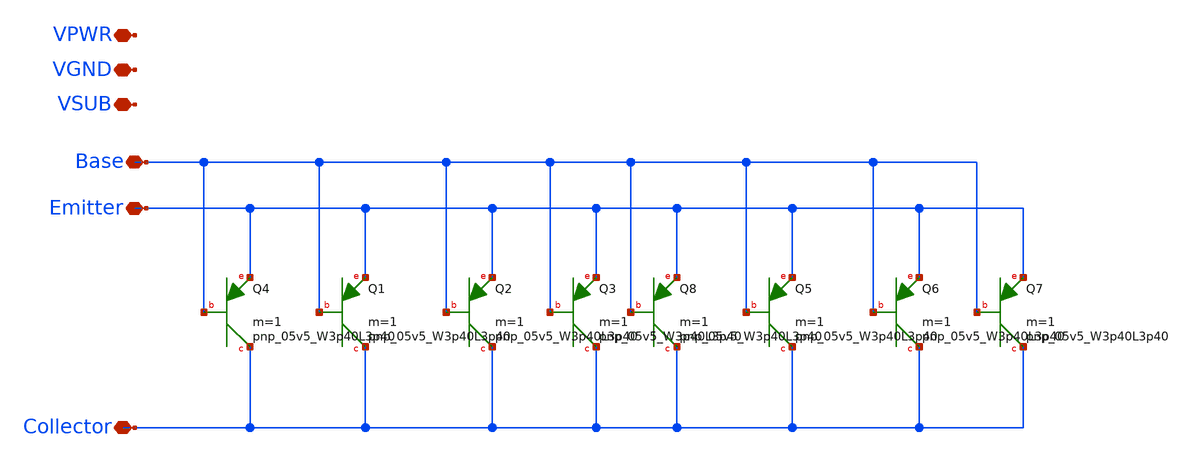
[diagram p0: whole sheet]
** sch_path: xschem/xschem/analog_stdcells/sky130_asc_pnp_05v5_W3p40L3p40_8.sch
**.subckt sky130_asc_pnp_05v5_W3p40L3p40_8 Base Emitter Collector VPWR VGND VSUB
*.iopin Base
*.iopin Emitter
*.iopin Collector
*.iopin VPWR
*.iopin VGND
*.iopin VSUB
XQ1 Collector Base Emitter sky130_fd_pr__pnp_05v5_W3p40L3p40 m=1
XQ2 Collector Base Emitter sky130_fd_pr__pnp_05v5_W3p40L3p40 m=1
XQ3 Collector Base Emitter sky130_fd_pr__pnp_05v5_W3p40L3p40 m=1
XQ4 Collector Base Emitter sky130_fd_pr__pnp_05v5_W3p40L3p40 m=1
XQ5 Collector Base Emitter sky130_fd_pr__pnp_05v5_W3p40L3p40 m=1
XQ6 Collector Base Emitter sky130_fd_pr__pnp_05v5_W3p40L3p40 m=1
XQ7 Collector Base Emitter sky130_fd_pr__pnp_05v5_W3p40L3p40 m=1
XQ8 Collector Base Emitter sky130_fd_pr__pnp_05v5_W3p40L3p40 m=1
**.ends
.end
